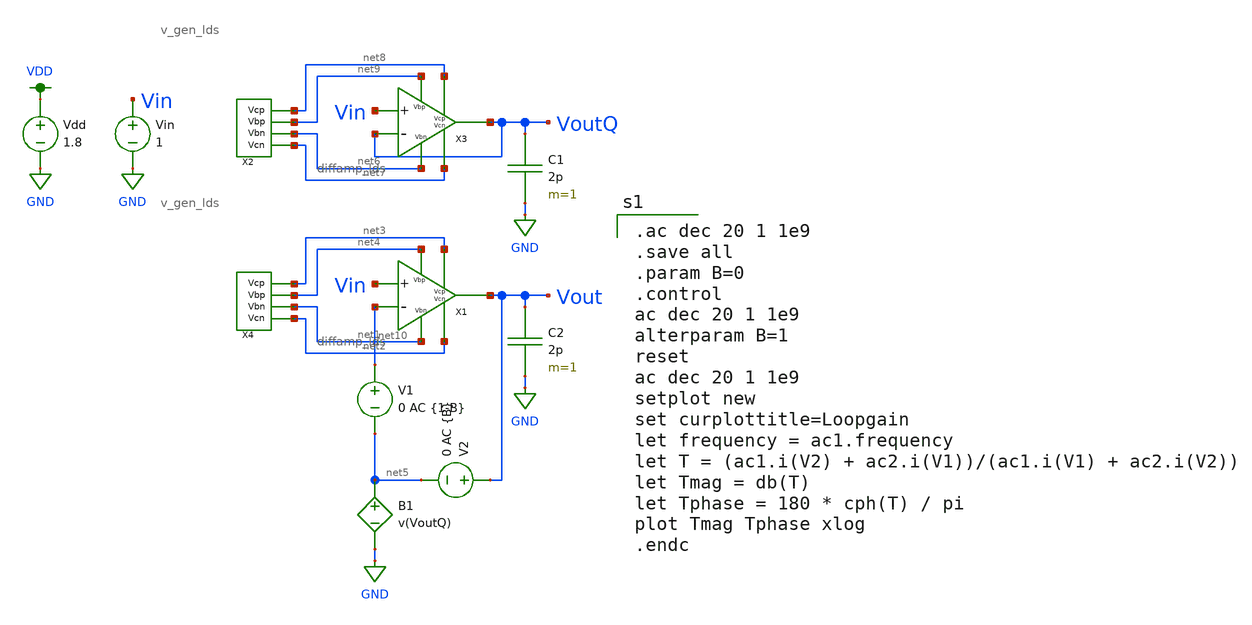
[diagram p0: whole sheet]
** sch_path: MP3/correction/xschem/final_loopgain.sch
**.subckt final_loopgain
Vdd VDD GND 1.8
Vin Vin GND 1
C2 Vout GND 2p m=1
V1 net10 net5 0 AC {1-B}
X1 net4 net1 net3 net2 Vin net10 Vout diffamp_lds
V2 Vout net5 0 AC {B}
B1 net5 GND V=v(VoutQ)
C1 VoutQ GND 2p m=1
X3 net9 net6 net8 net7 Vin VoutQ VoutQ diffamp_lds
X2 net8 net9 net6 net7 v_gen_lds
X4 net3 net4 net1 net2 v_gen_lds
**** begin user architecture code

.option wnflag=1
.lib ~/skywater/skywater-pdk/libraries/sky130_fd_pr_ngspice/latest/models/sky130.lib.spice tt


.ac dec 20 1 1e9
.save all
.param B=0
.control
ac dec 20 1 1e9
alterparam B=1
reset
ac dec 20 1 1e9
setplot new
set curplottitle=Loopgain
let frequency = ac1.frequency
let T = (ac1.i(V2) + ac2.i(V1))/(ac1.i(V1) + ac2.i(V2))
let Tmag = db(T)
let Tphase = 180 * cph(T) / pi
plot Tmag Tphase xlog
.endc

**** end user architecture code
**.ends

* expanding   symbol:  /home/madvlsi/MADVLSI_FA23/MP3/xschem/diffamp_lds.sym # of pins=7
** sym_path: MP3/correction/xschem/diffamp_lds.sym
** sch_path: MP3/correction/xschem/diffamp_lds.sch
.subckt diffamp_lds Vbp Vbn Vcp Vcn Vin Vref Vout
*.ipin Vin
*.ipin Vref
*.ipin Vbn
*.opin Vout
*.ipin Vbp
*.ipin Vcp
*.ipin Vcn
XM1 net1 Vin net2 GND sky130_fd_pr__nfet_01v8 L=0.5 W=12 nf=1 ad='int((nf+1)/2) * W/nf * 0.29' as='int((nf+2)/2) * W/nf * 0.29'
+ pd='2*int((nf+1)/2) * (W/nf + 0.29)' ps='2*int((nf+2)/2) * (W/nf + 0.29)' nrd='0.29 / W' nrs='0.29 / W'
+ sa=0 sb=0 sd=0 mult=1 m=1
XM2 net3 Vref net1 GND sky130_fd_pr__nfet_01v8 L=0.5 W=12 nf=1 ad='int((nf+1)/2) * W/nf * 0.29' as='int((nf+2)/2) * W/nf * 0.29'
+ pd='2*int((nf+1)/2) * (W/nf + 0.29)' ps='2*int((nf+2)/2) * (W/nf + 0.29)' nrd='0.29 / W' nrs='0.29 / W'
+ sa=0 sb=0 sd=0 mult=1 m=1
XMbn net1 Vbn GND GND sky130_fd_pr__nfet_01v8 L=0.5 W=12 nf=1 ad='int((nf+1)/2) * W/nf * 0.29' as='int((nf+2)/2) * W/nf * 0.29'
+ pd='2*int((nf+1)/2) * (W/nf + 0.29)' ps='2*int((nf+2)/2) * (W/nf + 0.29)' nrd='0.29 / W' nrs='0.29 / W'
+ sa=0 sb=0 sd=0 mult=1 m=1
XM3 VDD Vbp net2 VDD sky130_fd_pr__pfet_01v8 L=0.5 W=12 nf=1 ad='int((nf+1)/2) * W/nf * 0.29' as='int((nf+2)/2) * W/nf * 0.29'
+ pd='2*int((nf+1)/2) * (W/nf + 0.29)' ps='2*int((nf+2)/2) * (W/nf + 0.29)' nrd='0.29 / W' nrs='0.29 / W'
+ sa=0 sb=0 sd=0 mult=1 m=1
XM4 net3 Vbp VDD VDD sky130_fd_pr__pfet_01v8 L=0.5 W=12 nf=1 ad='int((nf+1)/2) * W/nf * 0.29' as='int((nf+2)/2) * W/nf * 0.29'
+ pd='2*int((nf+1)/2) * (W/nf + 0.29)' ps='2*int((nf+2)/2) * (W/nf + 0.29)' nrd='0.29 / W' nrs='0.29 / W'
+ sa=0 sb=0 sd=0 mult=1 m=1
XM5 net2 Vcp net5 VDD sky130_fd_pr__pfet_01v8 L=0.5 W=12 nf=1 ad='int((nf+1)/2) * W/nf * 0.29' as='int((nf+2)/2) * W/nf * 0.29'
+ pd='2*int((nf+1)/2) * (W/nf + 0.29)' ps='2*int((nf+2)/2) * (W/nf + 0.29)' nrd='0.29 / W' nrs='0.29 / W'
+ sa=0 sb=0 sd=0 mult=1 m=1
XM6 Vout Vcp net3 VDD sky130_fd_pr__pfet_01v8 L=0.5 W=12 nf=1 ad='int((nf+1)/2) * W/nf * 0.29' as='int((nf+2)/2) * W/nf * 0.29'
+ pd='2*int((nf+1)/2) * (W/nf + 0.29)' ps='2*int((nf+2)/2) * (W/nf + 0.29)' nrd='0.29 / W' nrs='0.29 / W'
+ sa=0 sb=0 sd=0 mult=1 m=1
XM7 net6 net5 GND GND sky130_fd_pr__nfet_01v8 L=0.5 W=12 nf=1 ad='int((nf+1)/2) * W/nf * 0.29' as='int((nf+2)/2) * W/nf * 0.29'
+ pd='2*int((nf+1)/2) * (W/nf + 0.29)' ps='2*int((nf+2)/2) * (W/nf + 0.29)' nrd='0.29 / W' nrs='0.29 / W'
+ sa=0 sb=0 sd=0 mult=1 m=1
XM8 GND net5 net4 GND sky130_fd_pr__nfet_01v8 L=0.5 W=12 nf=1 ad='int((nf+1)/2) * W/nf * 0.29' as='int((nf+2)/2) * W/nf * 0.29'
+ pd='2*int((nf+1)/2) * (W/nf + 0.29)' ps='2*int((nf+2)/2) * (W/nf + 0.29)' nrd='0.29 / W' nrs='0.29 / W'
+ sa=0 sb=0 sd=0 mult=1 m=1
XM9 net5 Vcn net6 GND sky130_fd_pr__nfet_01v8 L=0.5 W=12 nf=1 ad='int((nf+1)/2) * W/nf * 0.29' as='int((nf+2)/2) * W/nf * 0.29'
+ pd='2*int((nf+1)/2) * (W/nf + 0.29)' ps='2*int((nf+2)/2) * (W/nf + 0.29)' nrd='0.29 / W' nrs='0.29 / W'
+ sa=0 sb=0 sd=0 mult=1 m=1
XM10 net4 Vcn Vout GND sky130_fd_pr__nfet_01v8 L=0.5 W=12 nf=1 ad='int((nf+1)/2) * W/nf * 0.29' as='int((nf+2)/2) * W/nf * 0.29'
+ pd='2*int((nf+1)/2) * (W/nf + 0.29)' ps='2*int((nf+2)/2) * (W/nf + 0.29)' nrd='0.29 / W' nrs='0.29 / W'
+ sa=0 sb=0 sd=0 mult=1 m=1
XMdum GND GND net3 GND sky130_fd_pr__nfet_01v8 L=0.5 W=12 nf=1 ad='int((nf+1)/2) * W/nf * 0.29' as='int((nf+2)/2) * W/nf * 0.29'
+ pd='2*int((nf+1)/2) * (W/nf + 0.29)' ps='2*int((nf+2)/2) * (W/nf + 0.29)' nrd='0.29 / W' nrs='0.29 / W'
+ sa=0 sb=0 sd=0 mult=1 m=1
XM11 net7 Vin net8 GND sky130_fd_pr__nfet_01v8 L=0.5 W=12 nf=1 ad='int((nf+1)/2) * W/nf * 0.29' as='int((nf+2)/2) * W/nf * 0.29'
+ pd='2*int((nf+1)/2) * (W/nf + 0.29)' ps='2*int((nf+2)/2) * (W/nf + 0.29)' nrd='0.29 / W' nrs='0.29 / W'
+ sa=0 sb=0 sd=0 mult=1 m=1
XM12 net9 Vref net7 GND sky130_fd_pr__nfet_01v8 L=0.5 W=12 nf=1 ad='int((nf+1)/2) * W/nf * 0.29' as='int((nf+2)/2) * W/nf * 0.29'
+ pd='2*int((nf+1)/2) * (W/nf + 0.29)' ps='2*int((nf+2)/2) * (W/nf + 0.29)' nrd='0.29 / W' nrs='0.29 / W'
+ sa=0 sb=0 sd=0 mult=1 m=1
XMbn13 net7 Vbn GND GND sky130_fd_pr__nfet_01v8 L=0.5 W=12 nf=1 ad='int((nf+1)/2) * W/nf * 0.29' as='int((nf+2)/2) * W/nf * 0.29'
+ pd='2*int((nf+1)/2) * (W/nf + 0.29)' ps='2*int((nf+2)/2) * (W/nf + 0.29)' nrd='0.29 / W' nrs='0.29 / W'
+ sa=0 sb=0 sd=0 mult=1 m=1
XM14 VDD Vbp net8 VDD sky130_fd_pr__pfet_01v8 L=0.5 W=12 nf=1 ad='int((nf+1)/2) * W/nf * 0.29' as='int((nf+2)/2) * W/nf * 0.29'
+ pd='2*int((nf+1)/2) * (W/nf + 0.29)' ps='2*int((nf+2)/2) * (W/nf + 0.29)' nrd='0.29 / W' nrs='0.29 / W'
+ sa=0 sb=0 sd=0 mult=1 m=1
XM15 net9 Vbp VDD VDD sky130_fd_pr__pfet_01v8 L=0.5 W=12 nf=1 ad='int((nf+1)/2) * W/nf * 0.29' as='int((nf+2)/2) * W/nf * 0.29'
+ pd='2*int((nf+1)/2) * (W/nf + 0.29)' ps='2*int((nf+2)/2) * (W/nf + 0.29)' nrd='0.29 / W' nrs='0.29 / W'
+ sa=0 sb=0 sd=0 mult=1 m=1
XM16 net8 Vcp net5 VDD sky130_fd_pr__pfet_01v8 L=0.5 W=12 nf=1 ad='int((nf+1)/2) * W/nf * 0.29' as='int((nf+2)/2) * W/nf * 0.29'
+ pd='2*int((nf+1)/2) * (W/nf + 0.29)' ps='2*int((nf+2)/2) * (W/nf + 0.29)' nrd='0.29 / W' nrs='0.29 / W'
+ sa=0 sb=0 sd=0 mult=1 m=1
XM17 net10 Vcp net9 VDD sky130_fd_pr__pfet_01v8 L=0.5 W=12 nf=1 ad='int((nf+1)/2) * W/nf * 0.29' as='int((nf+2)/2) * W/nf * 0.29'
+ pd='2*int((nf+1)/2) * (W/nf + 0.29)' ps='2*int((nf+2)/2) * (W/nf + 0.29)' nrd='0.29 / W' nrs='0.29 / W'
+ sa=0 sb=0 sd=0 mult=1 m=1
XM18 net12 net5 GND GND sky130_fd_pr__nfet_01v8 L=0.5 W=12 nf=1 ad='int((nf+1)/2) * W/nf * 0.29' as='int((nf+2)/2) * W/nf * 0.29'
+ pd='2*int((nf+1)/2) * (W/nf + 0.29)' ps='2*int((nf+2)/2) * (W/nf + 0.29)' nrd='0.29 / W' nrs='0.29 / W'
+ sa=0 sb=0 sd=0 mult=1 m=1
XM19 GND net5 net11 GND sky130_fd_pr__nfet_01v8 L=0.5 W=12 nf=1 ad='int((nf+1)/2) * W/nf * 0.29' as='int((nf+2)/2) * W/nf * 0.29'
+ pd='2*int((nf+1)/2) * (W/nf + 0.29)' ps='2*int((nf+2)/2) * (W/nf + 0.29)' nrd='0.29 / W' nrs='0.29 / W'
+ sa=0 sb=0 sd=0 mult=1 m=1
XM20 net5 Vcn net12 GND sky130_fd_pr__nfet_01v8 L=0.5 W=12 nf=1 ad='int((nf+1)/2) * W/nf * 0.29' as='int((nf+2)/2) * W/nf * 0.29'
+ pd='2*int((nf+1)/2) * (W/nf + 0.29)' ps='2*int((nf+2)/2) * (W/nf + 0.29)' nrd='0.29 / W' nrs='0.29 / W'
+ sa=0 sb=0 sd=0 mult=1 m=1
XM21 net11 Vcn net10 GND sky130_fd_pr__nfet_01v8 L=0.5 W=12 nf=1 ad='int((nf+1)/2) * W/nf * 0.29' as='int((nf+2)/2) * W/nf * 0.29'
+ pd='2*int((nf+1)/2) * (W/nf + 0.29)' ps='2*int((nf+2)/2) * (W/nf + 0.29)' nrd='0.29 / W' nrs='0.29 / W'
+ sa=0 sb=0 sd=0 mult=1 m=1
XMdum22 GND GND net9 GND sky130_fd_pr__nfet_01v8 L=0.5 W=12 nf=1 ad='int((nf+1)/2) * W/nf * 0.29' as='int((nf+2)/2) * W/nf * 0.29'
+ pd='2*int((nf+1)/2) * (W/nf + 0.29)' ps='2*int((nf+2)/2) * (W/nf + 0.29)' nrd='0.29 / W' nrs='0.29 / W'
+ sa=0 sb=0 sd=0 mult=1 m=1
XMdum1 net10 GND GND GND sky130_fd_pr__nfet_01v8 L=0.5 W=12 nf=1 ad='int((nf+1)/2) * W/nf * 0.29' as='int((nf+2)/2) * W/nf * 0.29'
+ pd='2*int((nf+1)/2) * (W/nf + 0.29)' ps='2*int((nf+2)/2) * (W/nf + 0.29)' nrd='0.29 / W' nrs='0.29 / W'
+ sa=0 sb=0 sd=0 mult=1 m=1
XM13 VDD VDD net10 VDD sky130_fd_pr__pfet_01v8 L=0.5 W=12 nf=1 ad='int((nf+1)/2) * W/nf * 0.29' as='int((nf+2)/2) * W/nf * 0.29'
+ pd='2*int((nf+1)/2) * (W/nf + 0.29)' ps='2*int((nf+2)/2) * (W/nf + 0.29)' nrd='0.29 / W' nrs='0.29 / W'
+ sa=0 sb=0 sd=0 mult=1 m=1
XM22 net10 GND GND GND sky130_fd_pr__nfet_01v8 L=0.5 W=12 nf=1 ad='int((nf+1)/2) * W/nf * 0.29' as='int((nf+2)/2) * W/nf * 0.29'
+ pd='2*int((nf+1)/2) * (W/nf + 0.29)' ps='2*int((nf+2)/2) * (W/nf + 0.29)' nrd='0.29 / W' nrs='0.29 / W'
+ sa=0 sb=0 sd=0 mult=1 m=1
XMdum2 Vout GND GND GND sky130_fd_pr__nfet_01v8 L=0.5 W=12 nf=1 ad='int((nf+1)/2) * W/nf * 0.29' as='int((nf+2)/2) * W/nf * 0.29'
+ pd='2*int((nf+1)/2) * (W/nf + 0.29)' ps='2*int((nf+2)/2) * (W/nf + 0.29)' nrd='0.29 / W' nrs='0.29 / W'
+ sa=0 sb=0 sd=0 mult=1 m=1
XM23 VDD VDD Vout VDD sky130_fd_pr__pfet_01v8 L=0.5 W=12 nf=1 ad='int((nf+1)/2) * W/nf * 0.29' as='int((nf+2)/2) * W/nf * 0.29'
+ pd='2*int((nf+1)/2) * (W/nf + 0.29)' ps='2*int((nf+2)/2) * (W/nf + 0.29)' nrd='0.29 / W' nrs='0.29 / W'
+ sa=0 sb=0 sd=0 mult=1 m=1
XM24 Vout GND GND GND sky130_fd_pr__nfet_01v8 L=0.5 W=12 nf=1 ad='int((nf+1)/2) * W/nf * 0.29' as='int((nf+2)/2) * W/nf * 0.29'
+ pd='2*int((nf+1)/2) * (W/nf + 0.29)' ps='2*int((nf+2)/2) * (W/nf + 0.29)' nrd='0.29 / W' nrs='0.29 / W'
+ sa=0 sb=0 sd=0 mult=1 m=1
.ends


* expanding   symbol:  /home/madvlsi/MADVLSI_FA23/MP3/xschem/v_gen_lds.sym # of pins=4
** sym_path: MP3/correction/xschem/v_gen_lds.sym
** sch_path: MP3/correction/xschem/v_gen_lds.sch
.subckt v_gen_lds Vcp Vbp Vbn Vcn
*.opin Vcp
*.opin Vcn
*.opin Vbn
*.opin Vbp
XM29 VDD Vbp Vcn VDD sky130_fd_pr__pfet_01v8 L=0.5 W=12 nf=1 ad='int((nf+1)/2) * W/nf * 0.29' as='int((nf+2)/2) * W/nf * 0.29'
+ pd='2*int((nf+1)/2) * (W/nf + 0.29)' ps='2*int((nf+2)/2) * (W/nf + 0.29)' nrd='0.29 / W' nrs='0.29 / W'
+ sa=0 sb=0 sd=0 mult=1 m=1
XM30 Vcn Vcn net6 GND sky130_fd_pr__nfet_01v8 L=0.5 W=12 nf=1 ad='int((nf+1)/2) * W/nf * 0.29' as='int((nf+2)/2) * W/nf * 0.29'
+ pd='2*int((nf+1)/2) * (W/nf + 0.29)' ps='2*int((nf+2)/2) * (W/nf + 0.29)' nrd='0.29 / W' nrs='0.29 / W'
+ sa=0 sb=0 sd=0 mult=1 m=1
XM31 net1 Vbp VDD VDD sky130_fd_pr__pfet_01v8 L=0.5 W=12 nf=1 ad='int((nf+1)/2) * W/nf * 0.29' as='int((nf+2)/2) * W/nf * 0.29'
+ pd='2*int((nf+1)/2) * (W/nf + 0.29)' ps='2*int((nf+2)/2) * (W/nf + 0.29)' nrd='0.29 / W' nrs='0.29 / W'
+ sa=0 sb=0 sd=0 mult=1 m=1
XM32 net6 net5 net5 GND sky130_fd_pr__nfet_01v8 L=0.5 W=12 nf=1 ad='int((nf+1)/2) * W/nf * 0.29' as='int((nf+2)/2) * W/nf * 0.29'
+ pd='2*int((nf+1)/2) * (W/nf + 0.29)' ps='2*int((nf+2)/2) * (W/nf + 0.29)' nrd='0.29 / W' nrs='0.29 / W'
+ sa=0 sb=0 sd=0 mult=1 m=1
XM33 net2 Vbp net1 VDD sky130_fd_pr__pfet_01v8 L=0.5 W=12 nf=1 ad='int((nf+1)/2) * W/nf * 0.29' as='int((nf+2)/2) * W/nf * 0.29'
+ pd='2*int((nf+1)/2) * (W/nf + 0.29)' ps='2*int((nf+2)/2) * (W/nf + 0.29)' nrd='0.29 / W' nrs='0.29 / W'
+ sa=0 sb=0 sd=0 mult=1 m=1
XM34 net5 net5 net6 GND sky130_fd_pr__nfet_01v8 L=0.5 W=12 nf=1 ad='int((nf+1)/2) * W/nf * 0.29' as='int((nf+2)/2) * W/nf * 0.29'
+ pd='2*int((nf+1)/2) * (W/nf + 0.29)' ps='2*int((nf+2)/2) * (W/nf + 0.29)' nrd='0.29 / W' nrs='0.29 / W'
+ sa=0 sb=0 sd=0 mult=1 m=1
XM35 net3 Vbp net2 VDD sky130_fd_pr__pfet_01v8 L=0.5 W=12 nf=1 ad='int((nf+1)/2) * W/nf * 0.29' as='int((nf+2)/2) * W/nf * 0.29'
+ pd='2*int((nf+1)/2) * (W/nf + 0.29)' ps='2*int((nf+2)/2) * (W/nf + 0.29)' nrd='0.29 / W' nrs='0.29 / W'
+ sa=0 sb=0 sd=0 mult=1 m=1
XM36 net6 net5 net5 GND sky130_fd_pr__nfet_01v8 L=0.5 W=12 nf=1 ad='int((nf+1)/2) * W/nf * 0.29' as='int((nf+2)/2) * W/nf * 0.29'
+ pd='2*int((nf+1)/2) * (W/nf + 0.29)' ps='2*int((nf+2)/2) * (W/nf + 0.29)' nrd='0.29 / W' nrs='0.29 / W'
+ sa=0 sb=0 sd=0 mult=1 m=1
XM37 net4 Vbp net3 VDD sky130_fd_pr__pfet_01v8 L=0.5 W=12 nf=1 ad='int((nf+1)/2) * W/nf * 0.29' as='int((nf+2)/2) * W/nf * 0.29'
+ pd='2*int((nf+1)/2) * (W/nf + 0.29)' ps='2*int((nf+2)/2) * (W/nf + 0.29)' nrd='0.29 / W' nrs='0.29 / W'
+ sa=0 sb=0 sd=0 mult=1 m=1
XM38 net5 net5 net6 GND sky130_fd_pr__nfet_01v8 L=0.5 W=12 nf=1 ad='int((nf+1)/2) * W/nf * 0.29' as='int((nf+2)/2) * W/nf * 0.29'
+ pd='2*int((nf+1)/2) * (W/nf + 0.29)' ps='2*int((nf+2)/2) * (W/nf + 0.29)' nrd='0.29 / W' nrs='0.29 / W'
+ sa=0 sb=0 sd=0 mult=1 m=1
XM39 net5 Vbp net4 VDD sky130_fd_pr__pfet_01v8 L=0.5 W=12 nf=1 ad='int((nf+1)/2) * W/nf * 0.29' as='int((nf+2)/2) * W/nf * 0.29'
+ pd='2*int((nf+1)/2) * (W/nf + 0.29)' ps='2*int((nf+2)/2) * (W/nf + 0.29)' nrd='0.29 / W' nrs='0.29 / W'
+ sa=0 sb=0 sd=0 mult=1 m=1
XM40 net6 net5 GND GND sky130_fd_pr__nfet_01v8 L=0.5 W=12 nf=1 ad='int((nf+1)/2) * W/nf * 0.29' as='int((nf+2)/2) * W/nf * 0.29'
+ pd='2*int((nf+1)/2) * (W/nf + 0.29)' ps='2*int((nf+2)/2) * (W/nf + 0.29)' nrd='0.29 / W' nrs='0.29 / W'
+ sa=0 sb=0 sd=0 mult=1 m=1
XM25 net7 Vcp Vcp VDD sky130_fd_pr__pfet_01v8 L=0.5 W=12 nf=1 ad='int((nf+1)/2) * W/nf * 0.29' as='int((nf+2)/2) * W/nf * 0.29'
+ pd='2*int((nf+1)/2) * (W/nf + 0.29)' ps='2*int((nf+2)/2) * (W/nf + 0.29)' nrd='0.29 / W' nrs='0.29 / W'
+ sa=0 sb=0 sd=0 mult=1 m=1
XM26 Vcp Vbn GND GND sky130_fd_pr__nfet_01v8 L=0.5 W=12 nf=1 ad='int((nf+1)/2) * W/nf * 0.29' as='int((nf+2)/2) * W/nf * 0.29'
+ pd='2*int((nf+1)/2) * (W/nf + 0.29)' ps='2*int((nf+2)/2) * (W/nf + 0.29)' nrd='0.29 / W' nrs='0.29 / W'
+ sa=0 sb=0 sd=0 mult=1 m=1
XM27 net8 net8 net7 VDD sky130_fd_pr__pfet_01v8 L=0.5 W=12 nf=1 ad='int((nf+1)/2) * W/nf * 0.29' as='int((nf+2)/2) * W/nf * 0.29'
+ pd='2*int((nf+1)/2) * (W/nf + 0.29)' ps='2*int((nf+2)/2) * (W/nf + 0.29)' nrd='0.29 / W' nrs='0.29 / W'
+ sa=0 sb=0 sd=0 mult=1 m=1
XM28 GND Vbn net9 GND sky130_fd_pr__nfet_01v8 L=0.5 W=12 nf=1 ad='int((nf+1)/2) * W/nf * 0.29' as='int((nf+2)/2) * W/nf * 0.29'
+ pd='2*int((nf+1)/2) * (W/nf + 0.29)' ps='2*int((nf+2)/2) * (W/nf + 0.29)' nrd='0.29 / W' nrs='0.29 / W'
+ sa=0 sb=0 sd=0 mult=1 m=1
XM41 net7 net8 net8 VDD sky130_fd_pr__pfet_01v8 L=0.5 W=12 nf=1 ad='int((nf+1)/2) * W/nf * 0.29' as='int((nf+2)/2) * W/nf * 0.29'
+ pd='2*int((nf+1)/2) * (W/nf + 0.29)' ps='2*int((nf+2)/2) * (W/nf + 0.29)' nrd='0.29 / W' nrs='0.29 / W'
+ sa=0 sb=0 sd=0 mult=1 m=1
XM42 net9 Vbn net10 GND sky130_fd_pr__nfet_01v8 L=0.5 W=12 nf=1 ad='int((nf+1)/2) * W/nf * 0.29' as='int((nf+2)/2) * W/nf * 0.29'
+ pd='2*int((nf+1)/2) * (W/nf + 0.29)' ps='2*int((nf+2)/2) * (W/nf + 0.29)' nrd='0.29 / W' nrs='0.29 / W'
+ sa=0 sb=0 sd=0 mult=1 m=1
XM43 net8 net8 net7 VDD sky130_fd_pr__pfet_01v8 L=0.5 W=12 nf=1 ad='int((nf+1)/2) * W/nf * 0.29' as='int((nf+2)/2) * W/nf * 0.29'
+ pd='2*int((nf+1)/2) * (W/nf + 0.29)' ps='2*int((nf+2)/2) * (W/nf + 0.29)' nrd='0.29 / W' nrs='0.29 / W'
+ sa=0 sb=0 sd=0 mult=1 m=1
XM44 net10 Vbn net11 GND sky130_fd_pr__nfet_01v8 L=0.5 W=12 nf=1 ad='int((nf+1)/2) * W/nf * 0.29' as='int((nf+2)/2) * W/nf * 0.29'
+ pd='2*int((nf+1)/2) * (W/nf + 0.29)' ps='2*int((nf+2)/2) * (W/nf + 0.29)' nrd='0.29 / W' nrs='0.29 / W'
+ sa=0 sb=0 sd=0 mult=1 m=1
XM45 net7 net8 net8 VDD sky130_fd_pr__pfet_01v8 L=0.5 W=12 nf=1 ad='int((nf+1)/2) * W/nf * 0.29' as='int((nf+2)/2) * W/nf * 0.29'
+ pd='2*int((nf+1)/2) * (W/nf + 0.29)' ps='2*int((nf+2)/2) * (W/nf + 0.29)' nrd='0.29 / W' nrs='0.29 / W'
+ sa=0 sb=0 sd=0 mult=1 m=1
XM46 net11 Vbn net12 GND sky130_fd_pr__nfet_01v8 L=0.5 W=12 nf=1 ad='int((nf+1)/2) * W/nf * 0.29' as='int((nf+2)/2) * W/nf * 0.29'
+ pd='2*int((nf+1)/2) * (W/nf + 0.29)' ps='2*int((nf+2)/2) * (W/nf + 0.29)' nrd='0.29 / W' nrs='0.29 / W'
+ sa=0 sb=0 sd=0 mult=1 m=1
XM47 VDD net8 net7 VDD sky130_fd_pr__pfet_01v8 L=0.5 W=12 nf=1 ad='int((nf+1)/2) * W/nf * 0.29' as='int((nf+2)/2) * W/nf * 0.29'
+ pd='2*int((nf+1)/2) * (W/nf + 0.29)' ps='2*int((nf+2)/2) * (W/nf + 0.29)' nrd='0.29 / W' nrs='0.29 / W'
+ sa=0 sb=0 sd=0 mult=1 m=1
XM48 net12 Vbn net8 GND sky130_fd_pr__nfet_01v8 L=0.5 W=12 nf=1 ad='int((nf+1)/2) * W/nf * 0.29' as='int((nf+2)/2) * W/nf * 0.29'
+ pd='2*int((nf+1)/2) * (W/nf + 0.29)' ps='2*int((nf+2)/2) * (W/nf + 0.29)' nrd='0.29 / W' nrs='0.29 / W'
+ sa=0 sb=0 sd=0 mult=1 m=1
XM54 VDD Vbp Vbp VDD sky130_fd_pr__pfet_01v8 L=0.5 W=12 nf=1 ad='int((nf+1)/2) * W/nf * 0.29' as='int((nf+2)/2) * W/nf * 0.29'
+ pd='2*int((nf+1)/2) * (W/nf + 0.29)' ps='2*int((nf+2)/2) * (W/nf + 0.29)' nrd='0.29 / W' nrs='0.29 / W'
+ sa=0 sb=0 sd=0 mult=1 m=1
XM1 Vbp Vbn GND GND sky130_fd_pr__nfet_01v8 L=0.5 W=12 nf=1 ad='int((nf+1)/2) * W/nf * 0.29' as='int((nf+2)/2) * W/nf * 0.29'
+ pd='2*int((nf+1)/2) * (W/nf + 0.29)' ps='2*int((nf+2)/2) * (W/nf + 0.29)' nrd='0.29 / W' nrs='0.29 / W'
+ sa=0 sb=0 sd=0 mult=1 m=1
XM2 Vbn Vbn GND GND sky130_fd_pr__nfet_01v8 L=0.5 W=12 nf=1 ad='int((nf+1)/2) * W/nf * 0.29' as='int((nf+2)/2) * W/nf * 0.29'
+ pd='2*int((nf+1)/2) * (W/nf + 0.29)' ps='2*int((nf+2)/2) * (W/nf + 0.29)' nrd='0.29 / W' nrs='0.29 / W'
+ sa=0 sb=0 sd=0 mult=1 m=1
XM3 Vcp VDD VDD VDD sky130_fd_pr__pfet_01v8 L=0.5 W=12 nf=1 ad='int((nf+1)/2) * W/nf * 0.29' as='int((nf+2)/2) * W/nf * 0.29'
+ pd='2*int((nf+1)/2) * (W/nf + 0.29)' ps='2*int((nf+2)/2) * (W/nf + 0.29)' nrd='0.29 / W' nrs='0.29 / W'
+ sa=0 sb=0 sd=0 mult=1 m=1
XM4 VDD Vbp net24 VDD sky130_fd_pr__pfet_01v8 L=0.5 W=12 nf=1 ad='int((nf+1)/2) * W/nf * 0.29' as='int((nf+2)/2) * W/nf * 0.29'
+ pd='2*int((nf+1)/2) * (W/nf + 0.29)' ps='2*int((nf+2)/2) * (W/nf + 0.29)' nrd='0.29 / W' nrs='0.29 / W'
+ sa=0 sb=0 sd=0 mult=1 m=1
XM5 net24 net24 net17 GND sky130_fd_pr__nfet_01v8 L=0.5 W=12 nf=1 ad='int((nf+1)/2) * W/nf * 0.29' as='int((nf+2)/2) * W/nf * 0.29'
+ pd='2*int((nf+1)/2) * (W/nf + 0.29)' ps='2*int((nf+2)/2) * (W/nf + 0.29)' nrd='0.29 / W' nrs='0.29 / W'
+ sa=0 sb=0 sd=0 mult=1 m=1
XM6 net13 Vbp VDD VDD sky130_fd_pr__pfet_01v8 L=0.5 W=12 nf=1 ad='int((nf+1)/2) * W/nf * 0.29' as='int((nf+2)/2) * W/nf * 0.29'
+ pd='2*int((nf+1)/2) * (W/nf + 0.29)' ps='2*int((nf+2)/2) * (W/nf + 0.29)' nrd='0.29 / W' nrs='0.29 / W'
+ sa=0 sb=0 sd=0 mult=1 m=1
XM7 net17 net5 net5 GND sky130_fd_pr__nfet_01v8 L=0.5 W=12 nf=1 ad='int((nf+1)/2) * W/nf * 0.29' as='int((nf+2)/2) * W/nf * 0.29'
+ pd='2*int((nf+1)/2) * (W/nf + 0.29)' ps='2*int((nf+2)/2) * (W/nf + 0.29)' nrd='0.29 / W' nrs='0.29 / W'
+ sa=0 sb=0 sd=0 mult=1 m=1
XM8 net14 Vbp net13 VDD sky130_fd_pr__pfet_01v8 L=0.5 W=12 nf=1 ad='int((nf+1)/2) * W/nf * 0.29' as='int((nf+2)/2) * W/nf * 0.29'
+ pd='2*int((nf+1)/2) * (W/nf + 0.29)' ps='2*int((nf+2)/2) * (W/nf + 0.29)' nrd='0.29 / W' nrs='0.29 / W'
+ sa=0 sb=0 sd=0 mult=1 m=1
XM9 net5 net5 net17 GND sky130_fd_pr__nfet_01v8 L=0.5 W=12 nf=1 ad='int((nf+1)/2) * W/nf * 0.29' as='int((nf+2)/2) * W/nf * 0.29'
+ pd='2*int((nf+1)/2) * (W/nf + 0.29)' ps='2*int((nf+2)/2) * (W/nf + 0.29)' nrd='0.29 / W' nrs='0.29 / W'
+ sa=0 sb=0 sd=0 mult=1 m=1
XM10 net15 Vbp net14 VDD sky130_fd_pr__pfet_01v8 L=0.5 W=12 nf=1 ad='int((nf+1)/2) * W/nf * 0.29' as='int((nf+2)/2) * W/nf * 0.29'
+ pd='2*int((nf+1)/2) * (W/nf + 0.29)' ps='2*int((nf+2)/2) * (W/nf + 0.29)' nrd='0.29 / W' nrs='0.29 / W'
+ sa=0 sb=0 sd=0 mult=1 m=1
XM11 net17 net5 net5 GND sky130_fd_pr__nfet_01v8 L=0.5 W=12 nf=1 ad='int((nf+1)/2) * W/nf * 0.29' as='int((nf+2)/2) * W/nf * 0.29'
+ pd='2*int((nf+1)/2) * (W/nf + 0.29)' ps='2*int((nf+2)/2) * (W/nf + 0.29)' nrd='0.29 / W' nrs='0.29 / W'
+ sa=0 sb=0 sd=0 mult=1 m=1
XM12 net16 Vbp net15 VDD sky130_fd_pr__pfet_01v8 L=0.5 W=12 nf=1 ad='int((nf+1)/2) * W/nf * 0.29' as='int((nf+2)/2) * W/nf * 0.29'
+ pd='2*int((nf+1)/2) * (W/nf + 0.29)' ps='2*int((nf+2)/2) * (W/nf + 0.29)' nrd='0.29 / W' nrs='0.29 / W'
+ sa=0 sb=0 sd=0 mult=1 m=1
XM13 net5 net5 net17 GND sky130_fd_pr__nfet_01v8 L=0.5 W=12 nf=1 ad='int((nf+1)/2) * W/nf * 0.29' as='int((nf+2)/2) * W/nf * 0.29'
+ pd='2*int((nf+1)/2) * (W/nf + 0.29)' ps='2*int((nf+2)/2) * (W/nf + 0.29)' nrd='0.29 / W' nrs='0.29 / W'
+ sa=0 sb=0 sd=0 mult=1 m=1
XM14 net5 Vbp net16 VDD sky130_fd_pr__pfet_01v8 L=0.5 W=12 nf=1 ad='int((nf+1)/2) * W/nf * 0.29' as='int((nf+2)/2) * W/nf * 0.29'
+ pd='2*int((nf+1)/2) * (W/nf + 0.29)' ps='2*int((nf+2)/2) * (W/nf + 0.29)' nrd='0.29 / W' nrs='0.29 / W'
+ sa=0 sb=0 sd=0 mult=1 m=1
XM15 net17 net5 GND GND sky130_fd_pr__nfet_01v8 L=0.5 W=12 nf=1 ad='int((nf+1)/2) * W/nf * 0.29' as='int((nf+2)/2) * W/nf * 0.29'
+ pd='2*int((nf+1)/2) * (W/nf + 0.29)' ps='2*int((nf+2)/2) * (W/nf + 0.29)' nrd='0.29 / W' nrs='0.29 / W'
+ sa=0 sb=0 sd=0 mult=1 m=1
XM16 net18 net23 net23 VDD sky130_fd_pr__pfet_01v8 L=0.5 W=12 nf=1 ad='int((nf+1)/2) * W/nf * 0.29' as='int((nf+2)/2) * W/nf * 0.29'
+ pd='2*int((nf+1)/2) * (W/nf + 0.29)' ps='2*int((nf+2)/2) * (W/nf + 0.29)' nrd='0.29 / W' nrs='0.29 / W'
+ sa=0 sb=0 sd=0 mult=1 m=1
XM17 net23 Vbn GND GND sky130_fd_pr__nfet_01v8 L=0.5 W=12 nf=1 ad='int((nf+1)/2) * W/nf * 0.29' as='int((nf+2)/2) * W/nf * 0.29'
+ pd='2*int((nf+1)/2) * (W/nf + 0.29)' ps='2*int((nf+2)/2) * (W/nf + 0.29)' nrd='0.29 / W' nrs='0.29 / W'
+ sa=0 sb=0 sd=0 mult=1 m=1
XM18 net8 net8 net18 VDD sky130_fd_pr__pfet_01v8 L=0.5 W=12 nf=1 ad='int((nf+1)/2) * W/nf * 0.29' as='int((nf+2)/2) * W/nf * 0.29'
+ pd='2*int((nf+1)/2) * (W/nf + 0.29)' ps='2*int((nf+2)/2) * (W/nf + 0.29)' nrd='0.29 / W' nrs='0.29 / W'
+ sa=0 sb=0 sd=0 mult=1 m=1
XM19 GND Vbn net19 GND sky130_fd_pr__nfet_01v8 L=0.5 W=12 nf=1 ad='int((nf+1)/2) * W/nf * 0.29' as='int((nf+2)/2) * W/nf * 0.29'
+ pd='2*int((nf+1)/2) * (W/nf + 0.29)' ps='2*int((nf+2)/2) * (W/nf + 0.29)' nrd='0.29 / W' nrs='0.29 / W'
+ sa=0 sb=0 sd=0 mult=1 m=1
XM20 net18 net8 net8 VDD sky130_fd_pr__pfet_01v8 L=0.5 W=12 nf=1 ad='int((nf+1)/2) * W/nf * 0.29' as='int((nf+2)/2) * W/nf * 0.29'
+ pd='2*int((nf+1)/2) * (W/nf + 0.29)' ps='2*int((nf+2)/2) * (W/nf + 0.29)' nrd='0.29 / W' nrs='0.29 / W'
+ sa=0 sb=0 sd=0 mult=1 m=1
XM21 net19 Vbn net20 GND sky130_fd_pr__nfet_01v8 L=0.5 W=12 nf=1 ad='int((nf+1)/2) * W/nf * 0.29' as='int((nf+2)/2) * W/nf * 0.29'
+ pd='2*int((nf+1)/2) * (W/nf + 0.29)' ps='2*int((nf+2)/2) * (W/nf + 0.29)' nrd='0.29 / W' nrs='0.29 / W'
+ sa=0 sb=0 sd=0 mult=1 m=1
XM22 net8 net8 net18 VDD sky130_fd_pr__pfet_01v8 L=0.5 W=12 nf=1 ad='int((nf+1)/2) * W/nf * 0.29' as='int((nf+2)/2) * W/nf * 0.29'
+ pd='2*int((nf+1)/2) * (W/nf + 0.29)' ps='2*int((nf+2)/2) * (W/nf + 0.29)' nrd='0.29 / W' nrs='0.29 / W'
+ sa=0 sb=0 sd=0 mult=1 m=1
XM23 net20 Vbn net21 GND sky130_fd_pr__nfet_01v8 L=0.5 W=12 nf=1 ad='int((nf+1)/2) * W/nf * 0.29' as='int((nf+2)/2) * W/nf * 0.29'
+ pd='2*int((nf+1)/2) * (W/nf + 0.29)' ps='2*int((nf+2)/2) * (W/nf + 0.29)' nrd='0.29 / W' nrs='0.29 / W'
+ sa=0 sb=0 sd=0 mult=1 m=1
XM24 net18 net8 net8 VDD sky130_fd_pr__pfet_01v8 L=0.5 W=12 nf=1 ad='int((nf+1)/2) * W/nf * 0.29' as='int((nf+2)/2) * W/nf * 0.29'
+ pd='2*int((nf+1)/2) * (W/nf + 0.29)' ps='2*int((nf+2)/2) * (W/nf + 0.29)' nrd='0.29 / W' nrs='0.29 / W'
+ sa=0 sb=0 sd=0 mult=1 m=1
XM49 net21 Vbn net22 GND sky130_fd_pr__nfet_01v8 L=0.5 W=12 nf=1 ad='int((nf+1)/2) * W/nf * 0.29' as='int((nf+2)/2) * W/nf * 0.29'
+ pd='2*int((nf+1)/2) * (W/nf + 0.29)' ps='2*int((nf+2)/2) * (W/nf + 0.29)' nrd='0.29 / W' nrs='0.29 / W'
+ sa=0 sb=0 sd=0 mult=1 m=1
XM50 VDD net8 net18 VDD sky130_fd_pr__pfet_01v8 L=0.5 W=12 nf=1 ad='int((nf+1)/2) * W/nf * 0.29' as='int((nf+2)/2) * W/nf * 0.29'
+ pd='2*int((nf+1)/2) * (W/nf + 0.29)' ps='2*int((nf+2)/2) * (W/nf + 0.29)' nrd='0.29 / W' nrs='0.29 / W'
+ sa=0 sb=0 sd=0 mult=1 m=1
XM51 net22 Vbn net8 GND sky130_fd_pr__nfet_01v8 L=0.5 W=12 nf=1 ad='int((nf+1)/2) * W/nf * 0.29' as='int((nf+2)/2) * W/nf * 0.29'
+ pd='2*int((nf+1)/2) * (W/nf + 0.29)' ps='2*int((nf+2)/2) * (W/nf + 0.29)' nrd='0.29 / W' nrs='0.29 / W'
+ sa=0 sb=0 sd=0 mult=1 m=1
XM52 VDD Vbp Vbp VDD sky130_fd_pr__pfet_01v8 L=0.5 W=12 nf=1 ad='int((nf+1)/2) * W/nf * 0.29' as='int((nf+2)/2) * W/nf * 0.29'
+ pd='2*int((nf+1)/2) * (W/nf + 0.29)' ps='2*int((nf+2)/2) * (W/nf + 0.29)' nrd='0.29 / W' nrs='0.29 / W'
+ sa=0 sb=0 sd=0 mult=1 m=1
XM53 Vbp Vbn GND GND sky130_fd_pr__nfet_01v8 L=0.5 W=12 nf=1 ad='int((nf+1)/2) * W/nf * 0.29' as='int((nf+2)/2) * W/nf * 0.29'
+ pd='2*int((nf+1)/2) * (W/nf + 0.29)' ps='2*int((nf+2)/2) * (W/nf + 0.29)' nrd='0.29 / W' nrs='0.29 / W'
+ sa=0 sb=0 sd=0 mult=1 m=1
XM55 Vbn Vbn GND GND sky130_fd_pr__nfet_01v8 L=0.5 W=12 nf=1 ad='int((nf+1)/2) * W/nf * 0.29' as='int((nf+2)/2) * W/nf * 0.29'
+ pd='2*int((nf+1)/2) * (W/nf + 0.29)' ps='2*int((nf+2)/2) * (W/nf + 0.29)' nrd='0.29 / W' nrs='0.29 / W'
+ sa=0 sb=0 sd=0 mult=1 m=1
XM56 net23 VDD VDD VDD sky130_fd_pr__pfet_01v8 L=0.5 W=12 nf=1 ad='int((nf+1)/2) * W/nf * 0.29' as='int((nf+2)/2) * W/nf * 0.29'
+ pd='2*int((nf+1)/2) * (W/nf + 0.29)' ps='2*int((nf+2)/2) * (W/nf + 0.29)' nrd='0.29 / W' nrs='0.29 / W'
+ sa=0 sb=0 sd=0 mult=1 m=1
XM57 VDD VDD net23 VDD sky130_fd_pr__pfet_01v8 L=0.5 W=12 nf=1 ad='int((nf+1)/2) * W/nf * 0.29' as='int((nf+2)/2) * W/nf * 0.29'
+ pd='2*int((nf+1)/2) * (W/nf + 0.29)' ps='2*int((nf+2)/2) * (W/nf + 0.29)' nrd='0.29 / W' nrs='0.29 / W'
+ sa=0 sb=0 sd=0 mult=1 m=1
XM58 GND GND Vbn GND sky130_fd_pr__nfet_01v8 L=0.5 W=12 nf=1 ad='int((nf+1)/2) * W/nf * 0.29' as='int((nf+2)/2) * W/nf * 0.29'
+ pd='2*int((nf+1)/2) * (W/nf + 0.29)' ps='2*int((nf+2)/2) * (W/nf + 0.29)' nrd='0.29 / W' nrs='0.29 / W'
+ sa=0 sb=0 sd=0 mult=1 m=1
XM59 GND GND Vbp GND sky130_fd_pr__nfet_01v8 L=0.5 W=12 nf=1 ad='int((nf+1)/2) * W/nf * 0.29' as='int((nf+2)/2) * W/nf * 0.29'
+ pd='2*int((nf+1)/2) * (W/nf + 0.29)' ps='2*int((nf+2)/2) * (W/nf + 0.29)' nrd='0.29 / W' nrs='0.29 / W'
+ sa=0 sb=0 sd=0 mult=1 m=1
XM60 Vbp VDD VDD VDD sky130_fd_pr__pfet_01v8 L=0.5 W=12 nf=1 ad='int((nf+1)/2) * W/nf * 0.29' as='int((nf+2)/2) * W/nf * 0.29'
+ pd='2*int((nf+1)/2) * (W/nf + 0.29)' ps='2*int((nf+2)/2) * (W/nf + 0.29)' nrd='0.29 / W' nrs='0.29 / W'
+ sa=0 sb=0 sd=0 mult=1 m=1
XM61 VDD VDD Vcp VDD sky130_fd_pr__pfet_01v8 L=0.5 W=12 nf=1 ad='int((nf+1)/2) * W/nf * 0.29' as='int((nf+2)/2) * W/nf * 0.29'
+ pd='2*int((nf+1)/2) * (W/nf + 0.29)' ps='2*int((nf+2)/2) * (W/nf + 0.29)' nrd='0.29 / W' nrs='0.29 / W'
+ sa=0 sb=0 sd=0 mult=1 m=1
XM62 GND GND Vbn GND sky130_fd_pr__nfet_01v8 L=0.5 W=12 nf=1 ad='int((nf+1)/2) * W/nf * 0.29' as='int((nf+2)/2) * W/nf * 0.29'
+ pd='2*int((nf+1)/2) * (W/nf + 0.29)' ps='2*int((nf+2)/2) * (W/nf + 0.29)' nrd='0.29 / W' nrs='0.29 / W'
+ sa=0 sb=0 sd=0 mult=1 m=1
XM63 GND GND Vbp GND sky130_fd_pr__nfet_01v8 L=0.5 W=12 nf=1 ad='int((nf+1)/2) * W/nf * 0.29' as='int((nf+2)/2) * W/nf * 0.29'
+ pd='2*int((nf+1)/2) * (W/nf + 0.29)' ps='2*int((nf+2)/2) * (W/nf + 0.29)' nrd='0.29 / W' nrs='0.29 / W'
+ sa=0 sb=0 sd=0 mult=1 m=1
XM64 Vbp VDD VDD VDD sky130_fd_pr__pfet_01v8 L=0.5 W=12 nf=1 ad='int((nf+1)/2) * W/nf * 0.29' as='int((nf+2)/2) * W/nf * 0.29'
+ pd='2*int((nf+1)/2) * (W/nf + 0.29)' ps='2*int((nf+2)/2) * (W/nf + 0.29)' nrd='0.29 / W' nrs='0.29 / W'
+ sa=0 sb=0 sd=0 mult=1 m=1
.ends

.GLOBAL GND
.GLOBAL VDD
.end
